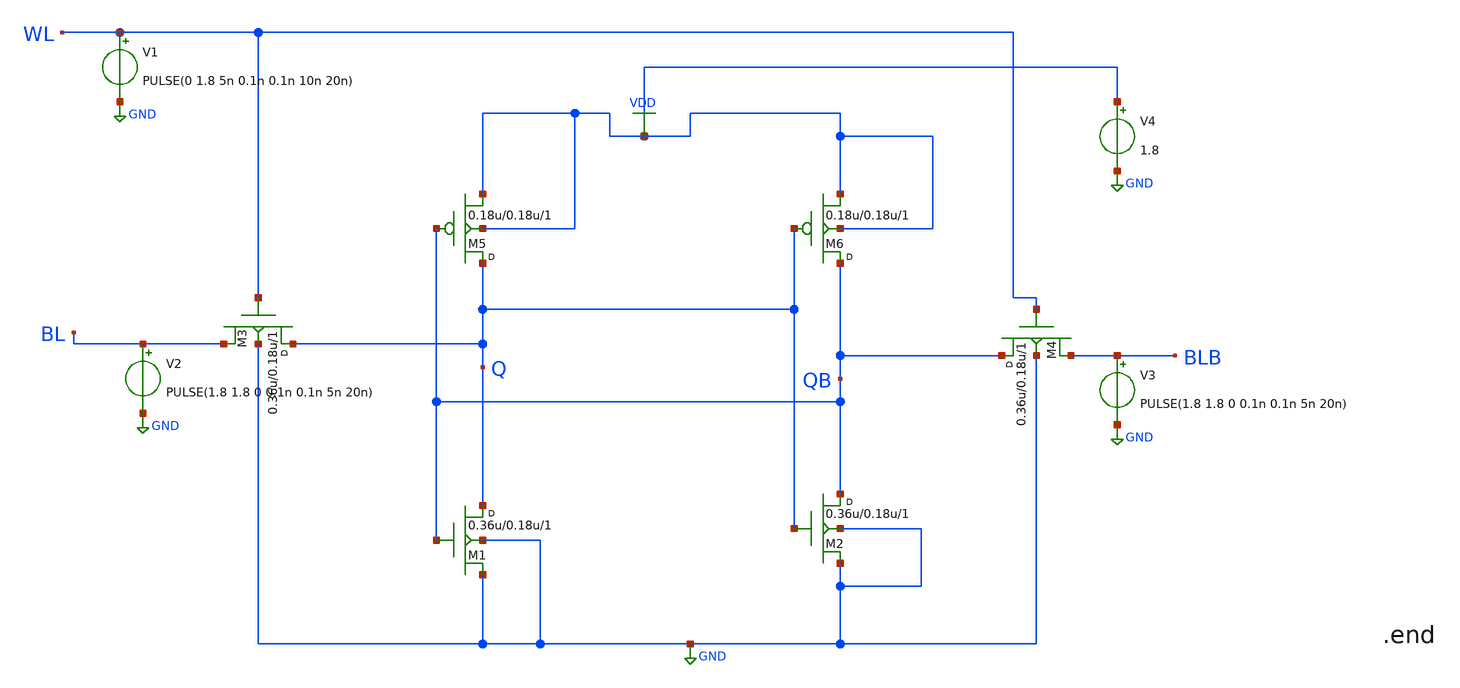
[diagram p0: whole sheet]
** sch_path: 6T SRAM/untitled-2.sch
**.subckt untitled-2
M1 Q QB GND GND nmos_model w=0.36u l=0.18u m=1
M2 QB Q GND GND nmos_model w=0.36u l=0.18u m=1
M3 Q WL BL GND nmos_model w=0.36u l=0.18u m=1
M4 QB WL BLB GND nmos_model w=0.36u l=0.18u m=1
M5 Q QB VDD VDD pmos_model w=0.18u l=0.18u m=1
M6 QB Q VDD VDD pmos_model w=0.18u l=0.18u m=1
V1 WL GND PULSE(0 1.8 5n 0.1n 0.1n 10n 20n)
V2 BL GND PULSE(1.8 1.8 0 0.1n 0.1n 5n 20n)
V3 BLB GND PULSE(1.8 1.8 0 0.1n 0.1n 5n 20n)
V4 VDD GND 1.8
**.ends
.GLOBAL GND
.GLOBAL VDD
.end
